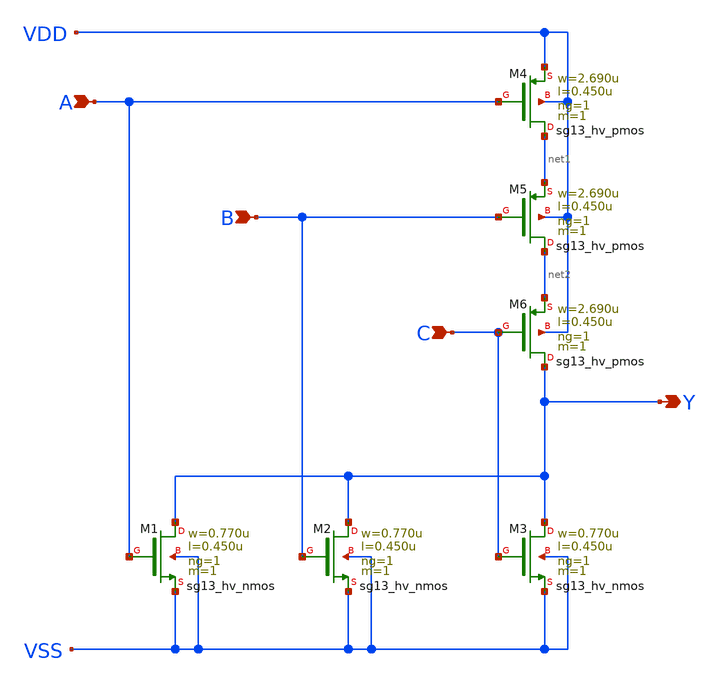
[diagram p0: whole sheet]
** sch_path: ihp-sg13g2/libs.ref/sg13g2_stdcell_hv/sch/xschem/sg13g2_hv_nor3_1.sch
* Copyright 2023 IHP PDK Authors
* Licensed under the Apache License, Version 2.0 (the "License");
* you may not use this file except in compliance with the License.
* You may obtain a copy of the License at
* https://www.apache.org/licenses/LICENSE-2.0
* Unless required by applicable law or agreed to in writing, software
* distributed under the License is distributed on an "AS IS" BASIS,
* WITHOUT WARRANTIES OR CONDITIONS OF ANY KIND, either express or implied.
* See the License for the specific language governing permissions and
* limitations under the License.
**.subckt sg13g2_hv_nor3_1 B Y A C
*.ipin B
*.opin Y
*.ipin A
*.ipin C
XM1 Y A VSS VSS sg13_hv_nmos w=0.770u l=0.450u ng=1 m=1 mm_ok=1
XM2 Y B VSS VSS sg13_hv_nmos w=0.770u l=0.450u ng=1 m=1 mm_ok=1
XM3 Y C VSS VSS sg13_hv_nmos w=0.770u l=0.450u ng=1 m=1 mm_ok=1
XM4 net1 A VDD VDD sg13_hv_pmos w=2.690u l=0.450u ng=1 m=1 mm_ok=1
XM5 net2 B net1 VDD sg13_hv_pmos w=2.690u l=0.450u ng=1 m=1 mm_ok=1
XM6 Y C net2 VDD sg13_hv_pmos w=2.690u l=0.450u ng=1 m=1 mm_ok=1
**.ends
.end
